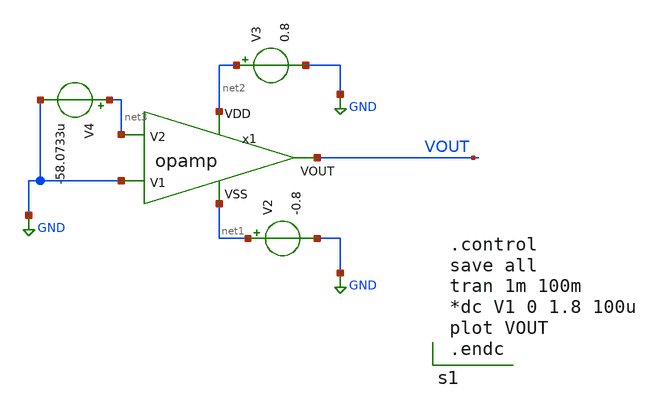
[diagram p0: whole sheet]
** sch_path: psrr.sch
**.subckt psrr
V3 net2 GND 0.8
V2 net1 GND -0.8
V4 net3 GND -58.0733u
x1 net2 net3 GND VOUT net1 opamp
**** begin user architecture code

** opencircuitdesign pdks install
.lib $::SKYWATER_MODELS/sky130.lib.spice tt




.control
save all
tran 1m 100m
*dc V1 0 1.8 100u
plot VOUT
.endc


**** end user architecture code
**.ends

* expanding   symbol:  /foss/designs/chipalooza2024/sky130_hcmus_ip__instramp/xschem/opamp.sym # of
*+ pins=5
** sym_path: opamp.sym
** sch_path: opamp.sch
.subckt opamp VDD V2 V1 VOUT VSS
*.ipin VSS
*.ipin VDD
*.ipin V2
*.ipin V1
*.opin VOUT
XM3 net4 V2 net1 VSS sky130_fd_pr__nfet_g5v0d10v5 L=1 W=17.45 nf=1 ad='int((nf+1)/2) * W/nf * 0.29' as='int((nf+2)/2) * W/nf * 0.29'
+ pd='2*int((nf+1)/2) * (W/nf + 0.29)' ps='2*int((nf+2)/2) * (W/nf + 0.29)' nrd='0.29 / W' nrs='0.29 / W'
+ sa=0 sb=0 sd=0 mult=1 m=1
XM1 net5 net4 VDD VDD sky130_fd_pr__pfet_g5v0d10v5 L=1 W=30 nf=1 ad='int((nf+1)/2) * W/nf * 0.29' as='int((nf+2)/2) * W/nf * 0.29'
+ pd='2*int((nf+1)/2) * (W/nf + 0.29)' ps='2*int((nf+2)/2) * (W/nf + 0.29)' nrd='0.29 / W' nrs='0.29 / W'
+ sa=0 sb=0 sd=0 mult=1 m=1
XM4 net5 V1 net1 VSS sky130_fd_pr__nfet_g5v0d10v5 L=1 W=17.45 nf=1 ad='int((nf+1)/2) * W/nf * 0.29' as='int((nf+2)/2) * W/nf * 0.29'
+ pd='2*int((nf+1)/2) * (W/nf + 0.29)' ps='2*int((nf+2)/2) * (W/nf + 0.29)' nrd='0.29 / W' nrs='0.29 / W'
+ sa=0 sb=0 sd=0 mult=1 m=1
XM6 net1 net6 VSS VSS sky130_fd_pr__nfet_g5v0d10v5 L=1 W=15.17 nf=1 ad='int((nf+1)/2) * W/nf * 0.29'
+ as='int((nf+2)/2) * W/nf * 0.29' pd='2*int((nf+1)/2) * (W/nf + 0.29)' ps='2*int((nf+2)/2) * (W/nf + 0.29)'
+ nrd='0.29 / W' nrs='0.29 / W' sa=0 sb=0 sd=0 mult=1 m=1
XM7 VOUT net6 VSS VSS sky130_fd_pr__nfet_g5v0d10v5 L=1 W=19 nf=1 ad='int((nf+1)/2) * W/nf * 0.29' as='int((nf+2)/2) * W/nf * 0.29'
+ pd='2*int((nf+1)/2) * (W/nf + 0.29)' ps='2*int((nf+2)/2) * (W/nf + 0.29)' nrd='0.29 / W' nrs='0.29 / W'
+ sa=0 sb=0 sd=0 mult=1 m=1
XM5 net6 net6 VSS VSS sky130_fd_pr__nfet_g5v0d10v5 L=1 W=15.17 nf=1 ad='int((nf+1)/2) * W/nf * 0.29'
+ as='int((nf+2)/2) * W/nf * 0.29' pd='2*int((nf+1)/2) * (W/nf + 0.29)' ps='2*int((nf+2)/2) * (W/nf + 0.29)'
+ nrd='0.29 / W' nrs='0.29 / W' sa=0 sb=0 sd=0 mult=1 m=1
XM2 net4 net4 VDD VDD sky130_fd_pr__pfet_g5v0d10v5 L=1 W=30 nf=1 ad='int((nf+1)/2) * W/nf * 0.29' as='int((nf+2)/2) * W/nf * 0.29'
+ pd='2*int((nf+1)/2) * (W/nf + 0.29)' ps='2*int((nf+2)/2) * (W/nf + 0.29)' nrd='0.29 / W' nrs='0.29 / W'
+ sa=0 sb=0 sd=0 mult=1 m=1
XM8 VOUT net5 VDD VDD sky130_fd_pr__pfet_g5v0d10v5 L=1 W=38 nf=1 ad='int((nf+1)/2) * W/nf * 0.29' as='int((nf+2)/2) * W/nf * 0.29'
+ pd='2*int((nf+1)/2) * (W/nf + 0.29)' ps='2*int((nf+2)/2) * (W/nf + 0.29)' nrd='0.29 / W' nrs='0.29 / W'
+ sa=0 sb=0 sd=0 mult=2 m=2
V_ibias net7 net6 0
.save i(v_ibias)
XR1 net2 VDD VSS sky130_fd_pr__res_high_po W=1 L=41.1 mult=1 m=1
XR2 net3 net2 VSS sky130_fd_pr__res_high_po W=1 L=41.1 mult=1 m=1
XR3 net7 net3 VSS sky130_fd_pr__res_high_po W=1 L=41.1 mult=1 m=1
XR4 net8 VOUT VSS sky130_fd_pr__res_high_po W=1 L=5 mult=1 m=1
XC1 net8 net5 sky130_fd_pr__cap_mim_m3_1 W=5 L=10 MF=10 m=10
.ends

.GLOBAL GND
.end
